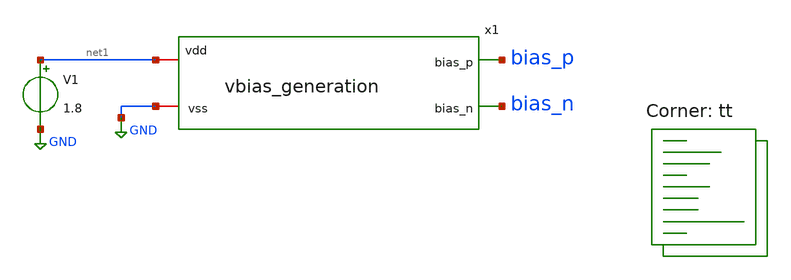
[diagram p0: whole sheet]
** sch_path: xsch/tb/vbias/bias_generation_tb.sch
**.subckt bias_generation_tb
x1 bias_n bias_p net1 GND vbias_generation
V1 net1 GND 1.8
**** begin user architecture code



* control language script

.control
dc V1 0 1.8 0.1
plot i(V1)
plot v(bias_p) v(bias_n)

.endc
.end



.lib $::SKYWATER_MODELS/sky130.lib.spice tt
**** end user architecture code
**.ends

* expanding   symbol:  /home/bmott/ttsky25b_tiny_chaos/xsch/ip/vbias_generation/vbias_generation.sym
*+ # of pins=4
** sym_path: xsch/ip/vbias_generation/vbias_generation.sym
** sch_path: xsch/ip/vbias_generation/vbias_generation.sch
.subckt vbias_generation bias_n bias_p vdd vss
*.opin bias_p
*.iopin vdd
*.iopin vss
*.opin bias_n
XR_bias_1 bias_1 bias_p vss sky130_fd_pr__res_xhigh_po_1p41 L=7 mult=1 m=1
XMn_bias bias_n bias_n vss vss sky130_fd_pr__nfet_01v8_lvt L=1 W=5 nf=1 ad='int((nf+1)/2) * W/nf * 0.29'
+ as='int((nf+2)/2) * W/nf * 0.29' pd='2*int((nf+1)/2) * (W/nf + 0.29)' ps='2*int((nf+2)/2) * (W/nf + 0.29)'
+ nrd='0.29 / W' nrs='0.29 / W' sa=0 sb=0 sd=0 mult=1 m=1
XMp_bias bias_p bias_p vdd vdd sky130_fd_pr__pfet_01v8_lvt L=1 W=10 nf=1 ad='int((nf+1)/2) * W/nf * 0.29'
+ as='int((nf+2)/2) * W/nf * 0.29' pd='2*int((nf+1)/2) * (W/nf + 0.29)' ps='2*int((nf+2)/2) * (W/nf + 0.29)'
+ nrd='0.29 / W' nrs='0.29 / W' sa=0 sb=0 sd=0 mult=1 m=1
XR_bias_2 bias_2 bias_1 vss sky130_fd_pr__res_xhigh_po_1p41 L=7 mult=1 m=1
XR_bias_3 bias_3 bias_2 vss sky130_fd_pr__res_xhigh_po_1p41 L=7 mult=1 m=1
XR_bias_4 bias_n bias_3 vss sky130_fd_pr__res_xhigh_po_1p41 L=7 mult=1 m=1
.ends

.GLOBAL GND
.end
